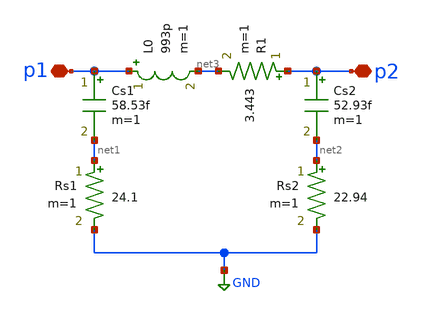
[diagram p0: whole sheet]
** sch_path: ask_modulator/xschem/l0.sch
**.subckt l0 p2 p1
*.iopin p2
*.iopin p1
L0 p1 net3 993p m=1
Cs1 p1 net1 58.53f m=1
Cs2 p2 net2 52.93f m=1
Rs1 net1 GND 24.1 m=1
Rs2 net2 GND 22.94 m=1
R1 p2 net3 3.443 m=1
**.ends
.GLOBAL GND
.end
